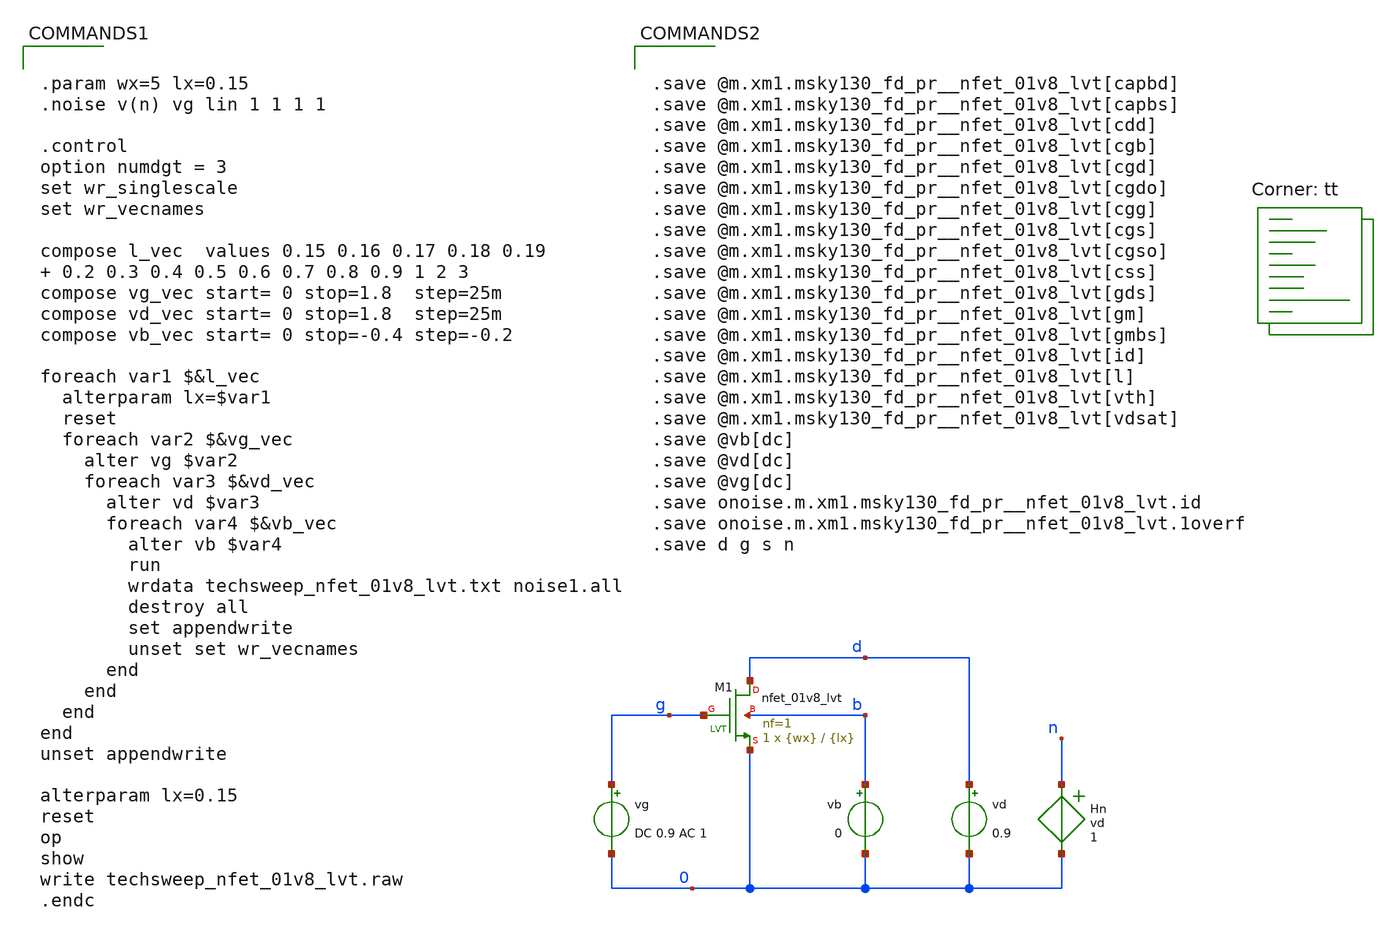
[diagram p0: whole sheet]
** sch_path: gmID-Design/Extraction/sky130A/techsweep_nfet_01v8_lvt.sch
**.subckt techsweep_nfet_01v8_lvt
vg g 0 DC 0.9 AC 1
vd d 0 0.9
vb b 0 0
XM1 d g 0 b sky130_fd_pr__nfet_01v8_lvt L={lx} W={wx} nf=1 ad='int((nf+1)/2) * W/nf * 0.29' as='int((nf+2)/2) * W/nf * 0.29'
+ pd='2*int((nf+1)/2) * (W/nf + 0.29)' ps='2*int((nf+2)/2) * (W/nf + 0.29)' nrd='0.29 / W' nrs='0.29 / W'
+ sa=0 sb=0 sd=0 mult=1 m=1
Hn n 0 vd 1
**** begin user architecture code


.param wx=5 lx=0.15
.noise v(n) vg lin 1 1 1 1

.control
option numdgt = 3
set wr_singlescale
set wr_vecnames

compose l_vec  values 0.15 0.16 0.17 0.18 0.19  0.2 0.3 0.4 0.5 0.6 0.7 0.8 0.9 1 2 3
compose vg_vec start= 0 stop=1.8  step=25m
compose vd_vec start= 0 stop=1.8  step=25m
compose vb_vec start= 0 stop=-0.4 step=-0.2

foreach var1 $&l_vec
  alterparam lx=$var1
  reset
  foreach var2 $&vg_vec
    alter vg $var2
    foreach var3 $&vd_vec
      alter vd $var3
      foreach var4 $&vb_vec
        alter vb $var4
        run
        wrdata techsweep_nfet_01v8_lvt.txt noise1.all
        destroy all
        set appendwrite
        unset set wr_vecnames
      end
    end
  end
end
unset appendwrite

alterparam lx=0.15
reset
op
show
write techsweep_nfet_01v8_lvt.raw
.endc


.lib $::SKYWATER_MODELS/sky130.lib.spice tt


.save @m.xm1.msky130_fd_pr__nfet_01v8_lvt[capbd]
.save @m.xm1.msky130_fd_pr__nfet_01v8_lvt[capbs]
.save @m.xm1.msky130_fd_pr__nfet_01v8_lvt[cdd]
.save @m.xm1.msky130_fd_pr__nfet_01v8_lvt[cgb]
.save @m.xm1.msky130_fd_pr__nfet_01v8_lvt[cgd]
.save @m.xm1.msky130_fd_pr__nfet_01v8_lvt[cgdo]
.save @m.xm1.msky130_fd_pr__nfet_01v8_lvt[cgg]
.save @m.xm1.msky130_fd_pr__nfet_01v8_lvt[cgs]
.save @m.xm1.msky130_fd_pr__nfet_01v8_lvt[cgso]
.save @m.xm1.msky130_fd_pr__nfet_01v8_lvt[css]
.save @m.xm1.msky130_fd_pr__nfet_01v8_lvt[gds]
.save @m.xm1.msky130_fd_pr__nfet_01v8_lvt[gm]
.save @m.xm1.msky130_fd_pr__nfet_01v8_lvt[gmbs]
.save @m.xm1.msky130_fd_pr__nfet_01v8_lvt[id]
.save @m.xm1.msky130_fd_pr__nfet_01v8_lvt[l]
.save @m.xm1.msky130_fd_pr__nfet_01v8_lvt[vth]
.save @m.xm1.msky130_fd_pr__nfet_01v8_lvt[vdsat]
.save @vb[dc]
.save @vd[dc]
.save @vg[dc]
.save onoise.m.xm1.msky130_fd_pr__nfet_01v8_lvt.id
.save onoise.m.xm1.msky130_fd_pr__nfet_01v8_lvt.1overf
.save d g s n


**** end user architecture code
**.ends
.end
